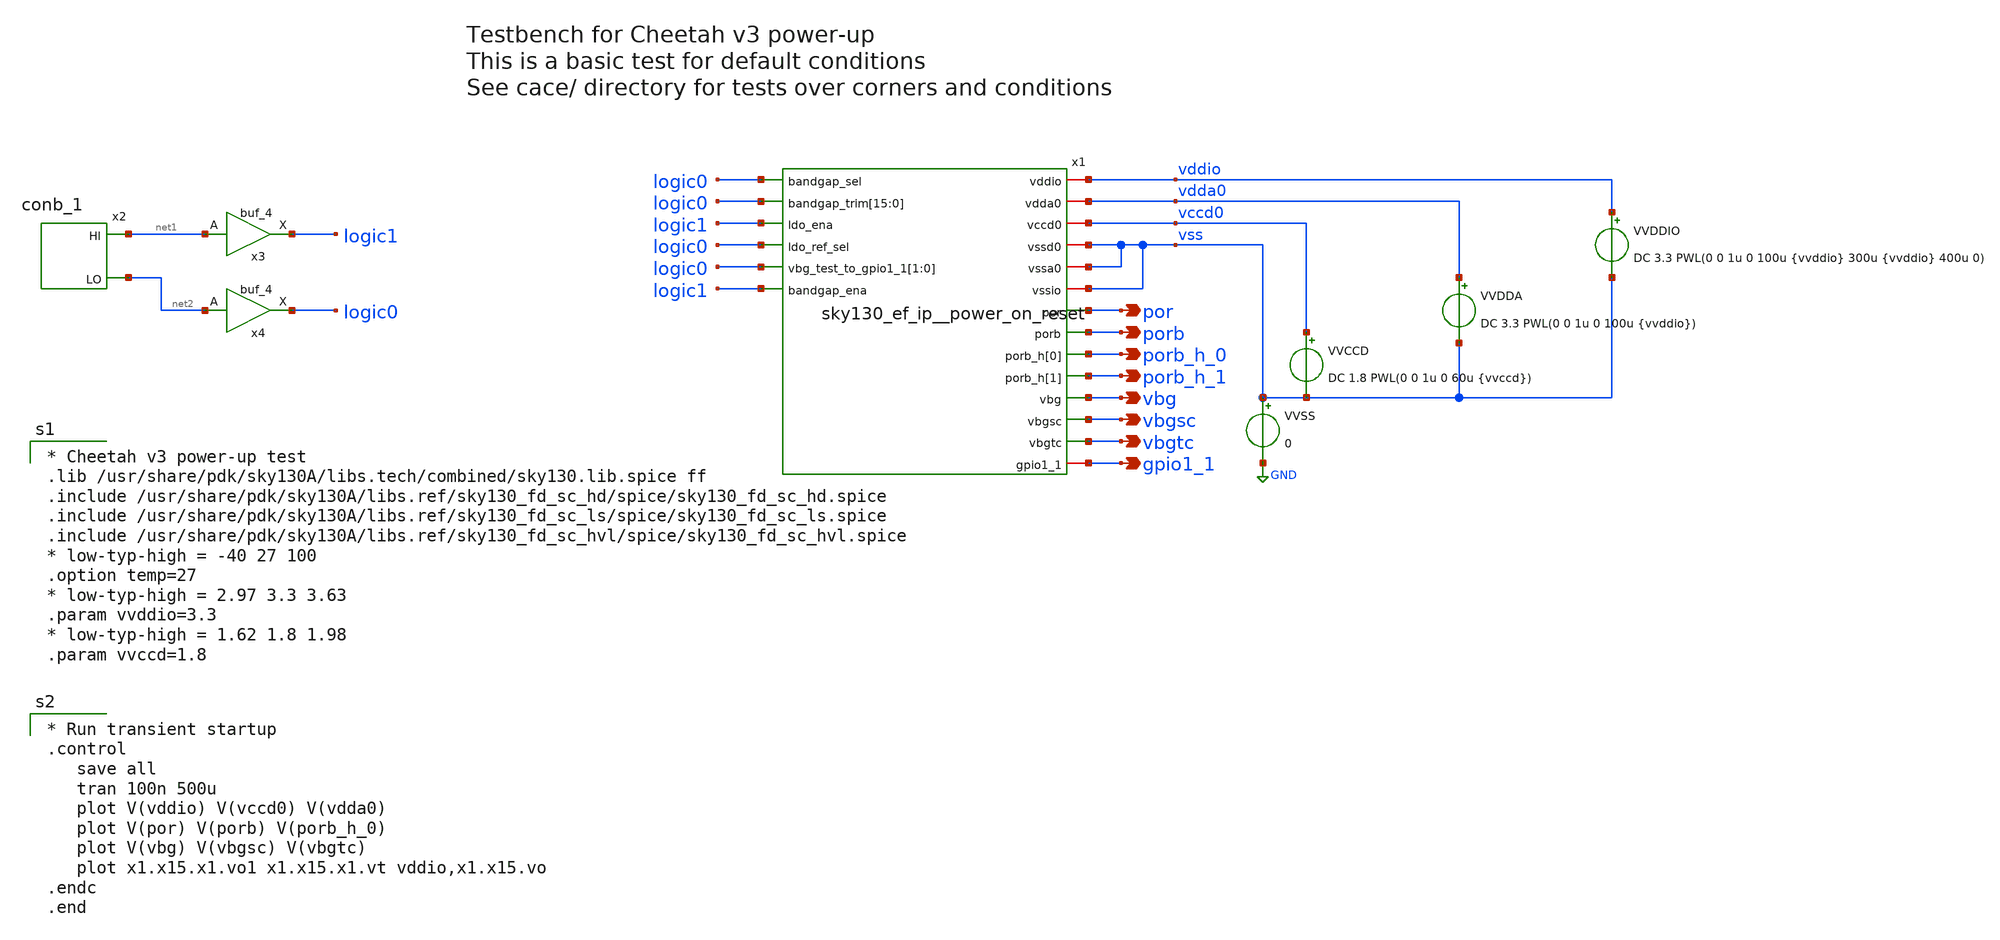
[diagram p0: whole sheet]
** sch_path: xschem/powerup_tb.sch
**.subckt powerup_tb por porb porb_h_0 vbg vbgsc vbgtc gpio1_1 porb_h_1
*.opin por
*.opin porb
*.opin porb_h_0
*.opin vbg
*.opin vbgsc
*.opin vbgtc
*.opin gpio1_1
*.opin porb_h_1
x1 vddio vdda0 vccd0 vss vss vss logic0 logic0 logic0 logic0 logic0 logic0 logic0 logic0 logic0
+ logic0 logic0 logic0 logic0 logic0 logic0 logic0 logic0 por porb porb_h_0 vbg vbgsc logic1 vbgtc logic0
+ gpio1_1 logic0 logic0 logic1 porb_h_1 sky130_ef_ip__power_on_reset
VVDDIO vddio vss DC 3.3 PWL(0 0 1u 0 100u {vvddio} 300u {vvddio} 400u 0)
VVDDA vdda0 vss DC 3.3 PWL(0 0 1u 0 100u {vvddio})
VVCCD vccd0 vss DC 1.8 PWL(0 0 1u 0 60u {vvccd})
x2 vss vss vccd0 vccd0 net1 net2 sky130_fd_sc_ls__conb_1
x3 net1 vss vss vccd0 vccd0 logic1 sky130_fd_sc_ls__buf_4
VVSS vss GND 0
x4 net2 vss vss vccd0 vccd0 logic0 sky130_fd_sc_ls__buf_4
**** begin user architecture code

* Cheetah v3 power-up test
.lib /usr/share/pdk/sky130A/libs.tech/combined/sky130.lib.spice ff
.include /usr/share/pdk/sky130A/libs.ref/sky130_fd_sc_hd/spice/sky130_fd_sc_hd.spice
.include /usr/share/pdk/sky130A/libs.ref/sky130_fd_sc_ls/spice/sky130_fd_sc_ls.spice
.include /usr/share/pdk/sky130A/libs.ref/sky130_fd_sc_hvl/spice/sky130_fd_sc_hvl.spice
* low-typ-high = -40 27 100
.option temp=27
* low-typ-high = 2.97 3.3 3.63
.param vvddio=3.3
* low-typ-high = 1.62 1.8 1.98
.param vvccd=1.8


* Run transient startup
.control
   save all
   tran 100n 500u
   plot V(vddio) V(vccd0) V(vdda0)
   plot V(por) V(porb) V(porb_h_0)
   plot V(vbg) V(vbgsc) V(vbgtc)
   plot x1.x15.x1.vo1 x1.x15.x1.vt vddio,x1.x15.vo
.endc
.end

**** end user architecture code
**.ends
.GLOBAL GND
.end
